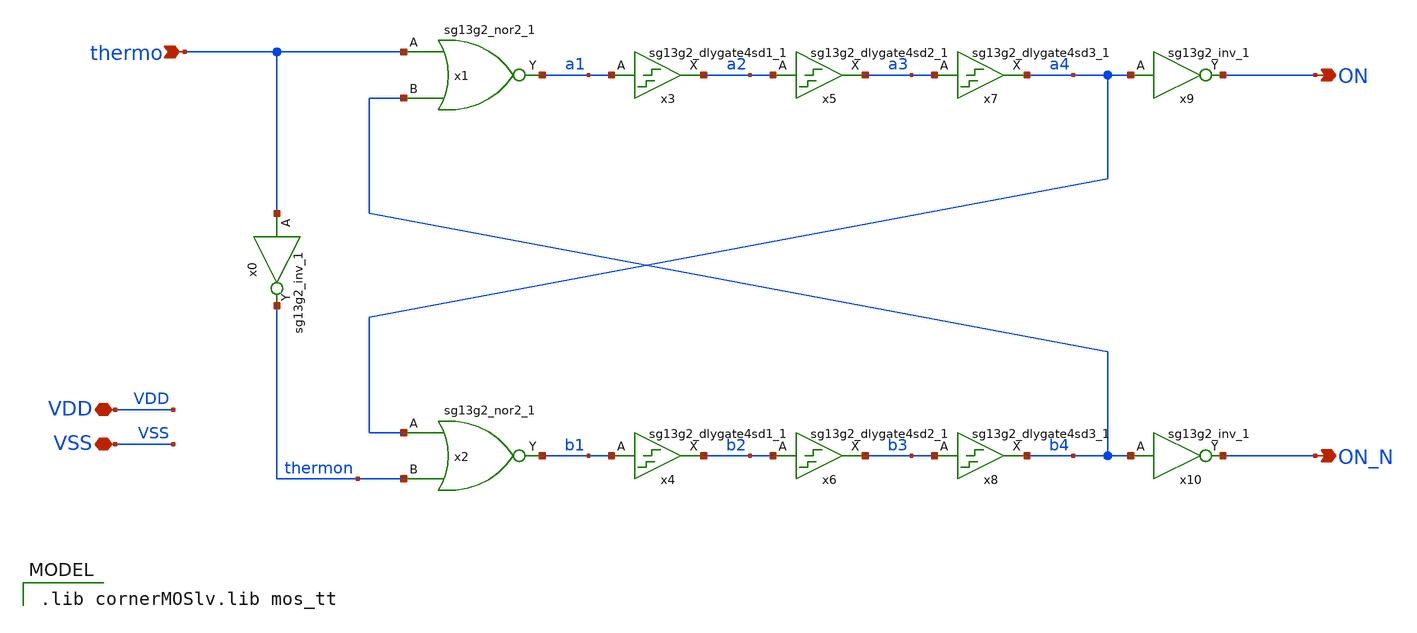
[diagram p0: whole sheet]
** sch_path: xschem/non_overlap.sch
* IHP-GmbH/IHP-Open-PDK/ihp-sg13g2/libs.tech/xschem/sg13g2_stdcells/sg13g2_dlygate4sd2_1.sch:
* Copyright 2023 IHP PDK Authors
* Licensed under the Apache License, Version 2.0 (the "License");
**.subckt non_overlap VSS thermo ON ON_N VDD
*.iopin VSS
*.ipin thermo
*.opin ON
*.opin ON_N
*.iopin VDD
x0 thermon thermo VDD VSS sg13g2_inv_1
x1 a1 thermo b4 VDD VSS sg13g2_nor2_1
x2 b1 a4 thermon VDD VSS sg13g2_nor2_1
x3 a2 a1 VDD VSS sg13g2_dlygate4sd1_1
x4 b2 b1 VDD VSS sg13g2_dlygate4sd1_1
x5 a3 a2 VDD VSS sg13g2_dlygate4sd2_1
x6 b3 b2 VDD VSS sg13g2_dlygate4sd2_1
x7 a4 a3 VDD VSS sg13g2_dlygate4sd3_1
x8 b4 b3 VDD VSS sg13g2_dlygate4sd3_1
x9 ON a4 VDD VSS sg13g2_inv_1
x10 ON_N b4 VDD VSS sg13g2_inv_1
**** begin user architecture code
 .lib cornerMOSlv.lib mos_tt

**** end user architecture code
**.ends

* expanding   symbol:  sg13g2_stdcells/sg13g2_inv_1.sym # of pins=2
** sym_path: sg13g2_stdcells/sg13g2_inv_1.sym
** sch_path: sg13g2_stdcells/sg13g2_inv_1.sch
.subckt sg13g2_inv_1 Y A VDD VSS
*.opin Y
*.ipin A
*.iopin VDD
*.iopin VSS
XM1 Y A VSS VSS sg13_lv_nmos w=740.00n l=130.00n ng=1 m=1 mm_ok=1
XM2 Y A VDD VDD sg13_lv_pmos w=1.12u l=130.00n ng=1 m=1 mm_ok=1
.ends


* expanding   symbol:  sg13g2_stdcells/sg13g2_nor2_1.sym # of pins=3
** sym_path: sg13g2_stdcells/sg13g2_nor2_1.sym
** sch_path: sg13g2_stdcells/sg13g2_nor2_1.sch
.subckt sg13g2_nor2_1 Y A B VDD VSS
*.opin Y
*.ipin B
*.ipin A
*.iopin VDD
*.iopin VSS
XM1 Y A VSS VSS sg13_lv_nmos w=740.00n l=130.00n ng=1 m=1 mm_ok=1
XM2 Y B VSS VSS sg13_lv_nmos w=740.00n l=130.00n ng=1 m=1 mm_ok=1
XM3 net1 A VDD VDD sg13_lv_pmos w=1.12u l=130.00n ng=1 m=1 mm_ok=1
XM4 Y B net1 VDD sg13_lv_pmos w=1.12u l=130.00n ng=1 m=1 mm_ok=1
.ends


* expanding   symbol:  sg13g2_stdcells/sg13g2_dlygate4sd1_1.sym # of pins=2
** sym_path: sg13g2_stdcells/sg13g2_dlygate4sd1_1.sym
** sch_path: sg13g2_stdcells/sg13g2_dlygate4sd1_1.sch
.subckt sg13g2_dlygate4sd1_1 X A VDD VSS
*.ipin A
*.opin X
*.iopin VDD
*.iopin VSS
XM1 net2 A VSS VSS sg13_lv_nmos w=420.00n l=130.00n ng=1 m=1 mm_ok=1
XM2 net1 net2 VSS VSS sg13_lv_nmos w=420.00n l=130.00n ng=1 m=1 mm_ok=1
XM3 net3 net1 VSS VSS sg13_lv_nmos w=420.00n l=130.00n ng=1 m=1 mm_ok=1
XM4 X net3 VSS VSS sg13_lv_nmos w=740.00n l=130.00n ng=1 m=1 mm_ok=1
XM5 net2 A VDD VDD sg13_lv_pmos w=420.00n l=130.00n ng=1 m=1 mm_ok=1
XM6 net1 net2 VDD VDD sg13_lv_pmos w=1.000u l=130.00n ng=1 m=1 mm_ok=1
XM7 net3 net1 VDD VDD sg13_lv_pmos w=1.000u l=130.00n ng=1 m=1 mm_ok=1
XM8 X net3 VDD VDD sg13_lv_pmos w=1.12u l=130.00n ng=1 m=1 mm_ok=1
.ends


* expanding   symbol:  sg13g2_stdcells/sg13g2_dlygate4sd2_1.sym # of pins=2
** sym_path: sg13g2_stdcells/sg13g2_dlygate4sd2_1.sym
** sch_path: sg13g2_stdcells/sg13g2_dlygate4sd2_1.sch
.subckt sg13g2_dlygate4sd2_1 X A VDD VSS
*.ipin A
*.opin X
*.iopin VDD
*.iopin VSS
XM1 net2 A VSS VSS sg13_lv_nmos w=420.00n l=130.00n ng=1 m=1 mm_ok=1
XM2 net1 net2 VSS VSS sg13_lv_nmos w=420.00n l=180.00n ng=1 m=1 mm_ok=1
XM3 net3 net1 VSS VSS sg13_lv_nmos w=420.00n l=180.00n ng=1 m=1 mm_ok=1
XM4 X net3 VSS VSS sg13_lv_nmos w=740.00n l=130.00n ng=1 m=1 mm_ok=1
XM5 net2 A VDD VDD sg13_lv_pmos w=420.00n l=130.00n ng=1 m=1 mm_ok=1
XM6 net1 net2 VDD VDD sg13_lv_pmos w=1.000u l=250.00n ng=1 m=1 mm_ok=1
XM7 net3 net1 VDD VDD sg13_lv_pmos w=1.000u l=250.00n ng=1 m=1 mm_ok=1
XM8 X net3 VDD VDD sg13_lv_pmos w=1.12u l=130.00n ng=1 m=1 mm_ok=1
.ends


* expanding   symbol:  sg13g2_stdcells/sg13g2_dlygate4sd3_1.sym # of pins=2
** sym_path: sg13g2_stdcells/sg13g2_dlygate4sd3_1.sym
** sch_path: sg13g2_stdcells/sg13g2_dlygate4sd3_1.sch
.subckt sg13g2_dlygate4sd3_1 X A VDD VSS
*.ipin A
*.opin X
*.iopin VDD
*.iopin VSS
XM1 net3 A VSS VSS sg13_lv_nmos w=420.00n l=130.00n ng=1 m=1 mm_ok=1
XM2 net1 net3 VSS VSS sg13_lv_nmos w=420.00n l=500.0n ng=1 m=1 mm_ok=1
XM3 net2 net1 VSS VSS sg13_lv_nmos w=420.00n l=500.0n ng=1 m=1 mm_ok=1
XM4 X net2 VSS VSS sg13_lv_nmos w=740.00n l=130.00n ng=1 m=1 mm_ok=1
XM5 net3 A VDD VDD sg13_lv_pmos w=420.00n l=130.00n ng=1 m=1 mm_ok=1
XM6 net1 net3 VDD VDD sg13_lv_pmos w=1.000u l=500.0n ng=1 m=1 mm_ok=1
XM7 net2 net1 VDD VDD sg13_lv_pmos w=1.000u l=500.0n ng=1 m=1 mm_ok=1
XM8 X net2 VDD VDD sg13_lv_pmos w=1.12u l=130.00n ng=1 m=1 mm_ok=1
.ends

.end
